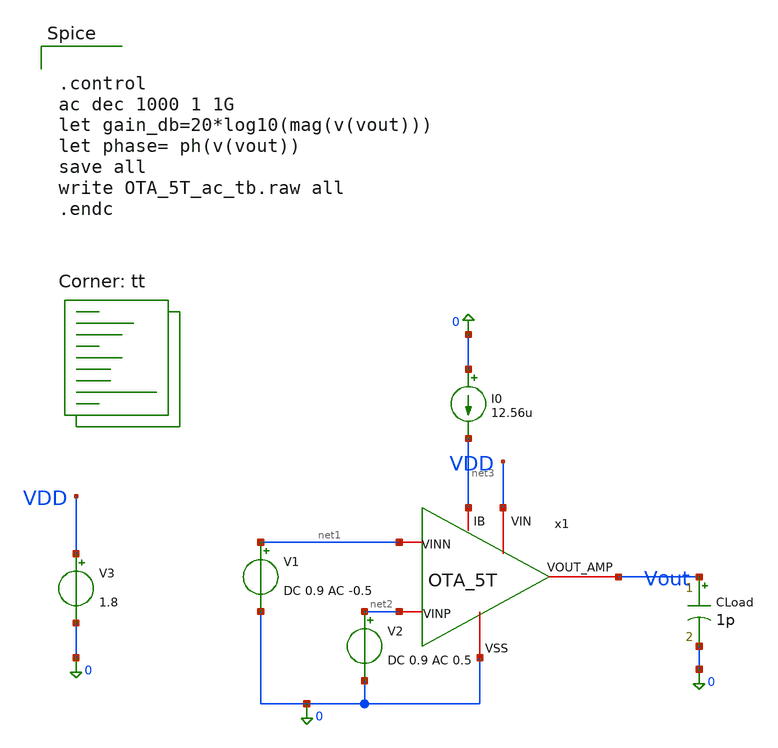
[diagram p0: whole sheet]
** sch_path: OTA_5T/OTA_5T_ac_tb.sch
**.subckt OTA_5T_ac_tb
V1 net1 0 DC 0.9 AC -0.5
V2 net2 0 DC 0.9 AC 0.5
V3 VDD 0 1.8
I0 0 net3 12.56u
CLoad Vout 0 1p m=1
x1 VDD Vout net1 net2 net3 0 OTA_5T
**** begin user architecture code
.lib $::SKYWATER_MODELS/sky130.lib.spice tt


.control
ac dec 1000 1 1G
let gain_db=20*log10(mag(v(vout)))
let phase= ph(v(vout))
save all
write OTA_5T_ac_tb.raw all
.endc


**** end user architecture code
**.ends

* expanding   symbol:  /foss/designs/Curso_Semiconductores/OTA_5T/OTA_5T.sym # of pins=6
** sym_path: /foss/designs/Curso_Semiconductores/OTA_5T/OTA_5T.sym
** sch_path: /foss/designs/Curso_Semiconductores/OTA_5T/OTA_5T.sch
.subckt OTA_5T VIN VOUT_AMP VINN VINP IB VSS
*.iopin VIN
*.iopin VSS
*.iopin VOUT_AMP
*.iopin IB
*.iopin VINN
*.iopin VINP
XM1 IB IB VSS VSS sky130_fd_pr__nfet_01v8 L=1 W=2.5 nf=1 ad='int((1 + 1)/2) * 2.5 / 1 * 0.29' as='int((1 + 2)/2) * 2.5 / 1 * 0.29'
+ pd='2*int((1 + 1)/2) * (2.5 / 1 + 0.29)' ps='2*int((1 + 2)/2) * (2.5 / 1 + 0.29)' nrd='0.29 / 2.5 ' nrs='0.29 / 2.5 '
+ sa=0 sb=0 sd=0 mult=4 m=4
XM2 tail IB VSS VSS sky130_fd_pr__nfet_01v8 L=1 W=2.5 nf=1 ad='int((1 + 1)/2) * 2.5 / 1 * 0.29' as='int((1 + 2)/2) * 2.5 / 1 * 0.29'
+ pd='2*int((1 + 1)/2) * (2.5 / 1 + 0.29)' ps='2*int((1 + 2)/2) * (2.5 / 1 + 0.29)' nrd='0.29 / 2.5 ' nrs='0.29 / 2.5 '
+ sa=0 sb=0 sd=0 mult=4 m=4
XM3 net1 VINP tail VSS sky130_fd_pr__nfet_01v8 L=1 W=3 nf=1 ad='int((1 + 1)/2) * 3 / 1 * 0.29' as='int((1 + 2)/2) * 3 / 1 * 0.29'
+ pd='2*int((1 + 1)/2) * (3 / 1 + 0.29)' ps='2*int((1 + 2)/2) * (3 / 1 + 0.29)' nrd='0.29 / 3 ' nrs='0.29 / 3 '
+ sa=0 sb=0 sd=0 mult=4 m=4
XM4 VOUT_AMP VINN tail VSS sky130_fd_pr__nfet_01v8 L=1 W=3 nf=1 ad='int((1 + 1)/2) * 3 / 1 * 0.29' as='int((1 + 2)/2) * 3 / 1 * 0.29'
+ pd='2*int((1 + 1)/2) * (3 / 1 + 0.29)' ps='2*int((1 + 2)/2) * (3 / 1 + 0.29)' nrd='0.29 / 3 ' nrs='0.29 / 3 '
+ sa=0 sb=0 sd=0 mult=4 m=4
XM5 VOUT_AMP net1 VIN VIN sky130_fd_pr__pfet_01v8 L=1 W=6 nf=1 ad='int((1 + 1)/2) * 6 / 1 * 0.29' as='int((1 + 2)/2) * 6 / 1 * 0.29'
+ pd='2*int((1 + 1)/2) * (6 / 1 + 0.29)' ps='2*int((1 + 2)/2) * (6 / 1 + 0.29)' nrd='0.29 / 6 ' nrs='0.29 / 6 '
+ sa=0 sb=0 sd=0 mult=4 m=4
XM6 net1 net1 VIN VIN sky130_fd_pr__pfet_01v8 L=1 W=6 nf=1 ad='int((1 + 1)/2) * 6 / 1 * 0.29' as='int((1 + 2)/2) * 6 / 1 * 0.29'
+ pd='2*int((1 + 1)/2) * (6 / 1 + 0.29)' ps='2*int((1 + 2)/2) * (6 / 1 + 0.29)' nrd='0.29 / 6 ' nrs='0.29 / 6 '
+ sa=0 sb=0 sd=0 mult=4 m=4
XD tail VSS tail VSS sky130_fd_pr__nfet_01v8 L=0.15 W=3 nf=1 ad='int((1 + 1)/2) * 3 / 1 * 0.29' as='int((1 + 2)/2) * 3 / 1 * 0.29'
+ pd='2*int((1 + 1)/2) * (3 / 1 + 0.29)' ps='2*int((1 + 2)/2) * (3 / 1 + 0.29)' nrd='0.29 / 3 ' nrs='0.29 / 3 '
+ sa=0 sb=0 sd=0 mult=4 m=4
XM7 VIN VIN VIN VIN sky130_fd_pr__pfet_01v8 L=0.15 W=6 nf=1 ad='int((1 + 1)/2) * 6 / 1 * 0.29' as='int((1 + 2)/2) * 6 / 1 * 0.29'
+ pd='2*int((1 + 1)/2) * (6 / 1 + 0.29)' ps='2*int((1 + 2)/2) * (6 / 1 + 0.29)' nrd='0.29 / 6 ' nrs='0.29 / 6 '
+ sa=0 sb=0 sd=0 mult=4 m=4
.ends

.end
